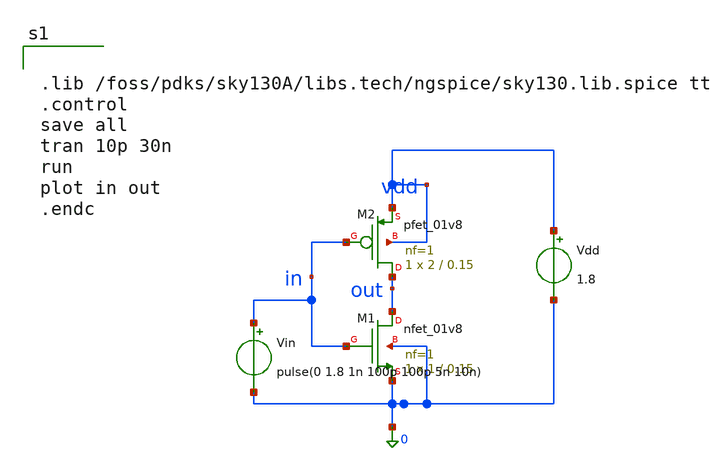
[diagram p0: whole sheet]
** sch_path: analog/cdac/inverter_demo.sch
**.subckt inverter_demo
XM1 out in 0 0 sky130_fd_pr__nfet_01v8 L=0.15 W=1 nf=1 ad='int((1 + 1)/2) * 1 / 1 * 0.29' as='int((1 + 2)/2) * 1 / 1 * 0.29'
+ pd='2*int((1 + 1)/2) * (1 / 1 + 0.29)' ps='2*int((1 + 2)/2) * (1 / 1 + 0.29)' nrd='0.29 / 1 ' nrs='0.29 / 1 '
+ sa=0 sb=0 sd=0 mult=1 m=1
XM2 out in vdd vdd sky130_fd_pr__pfet_01v8 L=0.15 W=2 nf=1 ad='int((1 + 1)/2) * 2 / 1 * 0.29' as='int((1 + 2)/2) * 2 / 1 * 0.29'
+ pd='2*int((1 + 1)/2) * (2 / 1 + 0.29)' ps='2*int((1 + 2)/2) * (2 / 1 + 0.29)' nrd='0.29 / 2 ' nrs='0.29 / 2 '
+ sa=0 sb=0 sd=0 mult=1 m=1
Vdd vdd 0 1.8
Vin in 0 pulse(0 1.8 1n 100p 100p 5n 10n)
**** begin user architecture code


.lib /foss/pdks/sky130A/libs.tech/ngspice/sky130.lib.spice tt
.control
save all
tran 10p 30n
run
plot in out
.endc

**** end user architecture code
**.ends
.end
